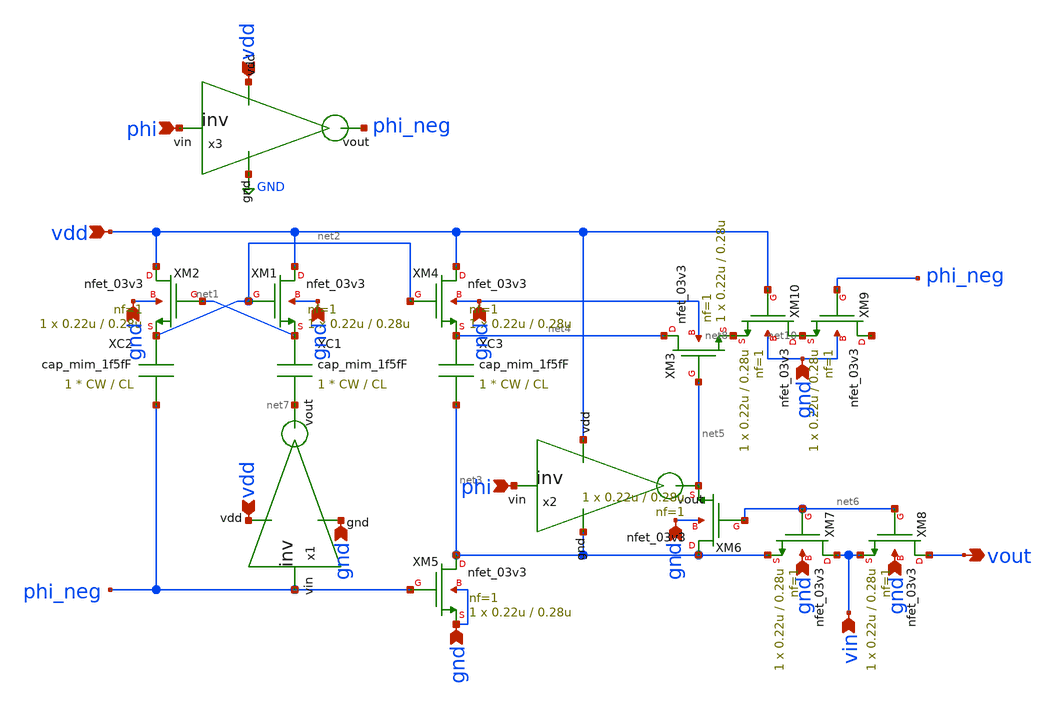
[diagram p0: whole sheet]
** sch_path: symbols/bootstrap_sw.sch
**.subckt bootstrap_sw phi vdd vdd phi vin vout vdd gnd gnd gnd gnd gnd gnd gnd gnd gnd
*.ipin phi
*.ipin vdd
*.ipin vdd
*.ipin phi
*.ipin vin
*.opin vout
*.ipin vdd
*.ipin gnd
*.ipin gnd
*.ipin gnd
*.ipin gnd
*.ipin gnd
*.ipin gnd
*.ipin gnd
*.ipin gnd
*.ipin gnd
x1 vdd gnd net7 phi_neg inv cl=0.28u wp=0.44u wn=0.22u
XC1 net1 net7 cap_mim_1f5fF c_width=CW c_length=CL m=1
XC2 net2 phi_neg cap_mim_1f5fF c_width=CW c_length=CL m=1
XM1 vdd net2 net1 gnd nfet_03v3 L=0.28u W=0.22u nf=1 ad='int((nf+1)/2) * W/nf * 0.18u' as='int((nf+2)/2) * W/nf * 0.18u'
+ pd='2*int((nf+1)/2) * (W/nf + 0.18u)' ps='2*int((nf+2)/2) * (W/nf + 0.18u)' nrd='0.18u / W' nrs='0.18u / W'
+ sa=0 sb=0 sd=0 m=1
XM2 vdd net1 net2 gnd nfet_03v3 L=0.28u W=0.22u nf=1 ad='int((nf+1)/2) * W/nf * 0.18u' as='int((nf+2)/2) * W/nf * 0.18u'
+ pd='2*int((nf+1)/2) * (W/nf + 0.18u)' ps='2*int((nf+2)/2) * (W/nf + 0.18u)' nrd='0.18u / W' nrs='0.18u / W'
+ sa=0 sb=0 sd=0 m=1
XM4 vdd net2 net4 gnd nfet_03v3 L=0.28u W=0.22u nf=1 ad='int((nf+1)/2) * W/nf * 0.18u' as='int((nf+2)/2) * W/nf * 0.18u'
+ pd='2*int((nf+1)/2) * (W/nf + 0.18u)' ps='2*int((nf+2)/2) * (W/nf + 0.18u)' nrd='0.18u / W' nrs='0.18u / W'
+ sa=0 sb=0 sd=0 m=1
XC3 net4 net3 cap_mim_1f5fF c_width=CW c_length=CL m=1
XM5 net3 phi_neg gnd gnd nfet_03v3 L=0.28u W=0.22u nf=1 ad='int((nf+1)/2) * W/nf * 0.18u' as='int((nf+2)/2) * W/nf * 0.18u'
+ pd='2*int((nf+1)/2) * (W/nf + 0.18u)' ps='2*int((nf+2)/2) * (W/nf + 0.18u)' nrd='0.18u / W' nrs='0.18u / W'
+ sa=0 sb=0 sd=0 m=1
x2 vdd net3 net5 phi inv cl=0.28u wp=0.44u wn=0.22u
x3 vdd GND phi_neg phi inv cl=0.28u wp=0.44u wn=0.22u
XM3 net4 net5 net8 gnd nfet_03v3 L=0.28u W=0.22u nf=1 ad='int((nf+1)/2) * W/nf * 0.18u' as='int((nf+2)/2) * W/nf * 0.18u'
+ pd='2*int((nf+1)/2) * (W/nf + 0.18u)' ps='2*int((nf+2)/2) * (W/nf + 0.18u)' nrd='0.18u / W' nrs='0.18u / W'
+ sa=0 sb=0 sd=0 m=1
XM6 net3 net6 net5 gnd nfet_03v3 L=0.28u W=0.22u nf=1 ad='int((nf+1)/2) * W/nf * 0.18u' as='int((nf+2)/2) * W/nf * 0.18u'
+ pd='2*int((nf+1)/2) * (W/nf + 0.18u)' ps='2*int((nf+2)/2) * (W/nf + 0.18u)' nrd='0.18u / W' nrs='0.18u / W'
+ sa=0 sb=0 sd=0 m=1
XM7 vin net6 net3 gnd nfet_03v3 L=0.28u W=0.22u nf=1 ad='int((nf+1)/2) * W/nf * 0.18u' as='int((nf+2)/2) * W/nf * 0.18u'
+ pd='2*int((nf+1)/2) * (W/nf + 0.18u)' ps='2*int((nf+2)/2) * (W/nf + 0.18u)' nrd='0.18u / W' nrs='0.18u / W'
+ sa=0 sb=0 sd=0 m=1
XM8 vout net6 vin gnd nfet_03v3 L=0.28u W=0.22u nf=1 ad='int((nf+1)/2) * W/nf * 0.18u' as='int((nf+2)/2) * W/nf * 0.18u'
+ pd='2*int((nf+1)/2) * (W/nf + 0.18u)' ps='2*int((nf+2)/2) * (W/nf + 0.18u)' nrd='0.18u / W' nrs='0.18u / W'
+ sa=0 sb=0 sd=0 m=1
XM9 net9 phi_neg net10 gnd nfet_03v3 L=0.28u W=0.22u nf=1 ad='int((nf+1)/2) * W/nf * 0.18u' as='int((nf+2)/2) * W/nf * 0.18u'
+ pd='2*int((nf+1)/2) * (W/nf + 0.18u)' ps='2*int((nf+2)/2) * (W/nf + 0.18u)' nrd='0.18u / W' nrs='0.18u / W'
+ sa=0 sb=0 sd=0 m=1
XM10 net10 vdd net8 gnd nfet_03v3 L=0.28u W=0.22u nf=1 ad='int((nf+1)/2) * W/nf * 0.18u' as='int((nf+2)/2) * W/nf * 0.18u'
+ pd='2*int((nf+1)/2) * (W/nf + 0.18u)' ps='2*int((nf+2)/2) * (W/nf + 0.18u)' nrd='0.18u / W' nrs='0.18u / W'
+ sa=0 sb=0 sd=0 m=1
**.ends

* expanding   symbol:  /foss/designs/sar_adc/xschem/spice/inv.sym # of pins=4
** sym_path: /foss/designs/sar_adc/xschem/spice/inv.sym
** sch_path: /foss/designs/sar_adc/xschem/spice/inv.sch
.subckt inv vdd gnd vout vin  cl=0.28u wp=0.44u wn=0.22u
*.ipin gnd
*.ipin vdd
*.ipin vin
*.opin vout
XM1 gnd vin vout gnd nfet_03v3 L=0.28u W=.22u nf=1 ad='int((nf+1)/2) * W/nf * 0.18u' as='int((nf+2)/2) * W/nf * 0.18u'
+ pd='2*int((nf+1)/2) * (W/nf + 0.18u)' ps='2*int((nf+2)/2) * (W/nf + 0.18u)' nrd='0.18u / W' nrs='0.18u / W'
+ sa=0 sb=0 sd=0 m=1
XM2 vdd vin vout vdd pfet_03v3 L=0.28u W=.22u nf=1 ad='int((nf+1)/2) * W/nf * 0.18u' as='int((nf+2)/2) * W/nf * 0.18u'
+ pd='2*int((nf+1)/2) * (W/nf + 0.18u)' ps='2*int((nf+2)/2) * (W/nf + 0.18u)' nrd='0.18u / W' nrs='0.18u / W'
+ sa=0 sb=0 sd=0 m=1
.ends

.GLOBAL GND
.end
